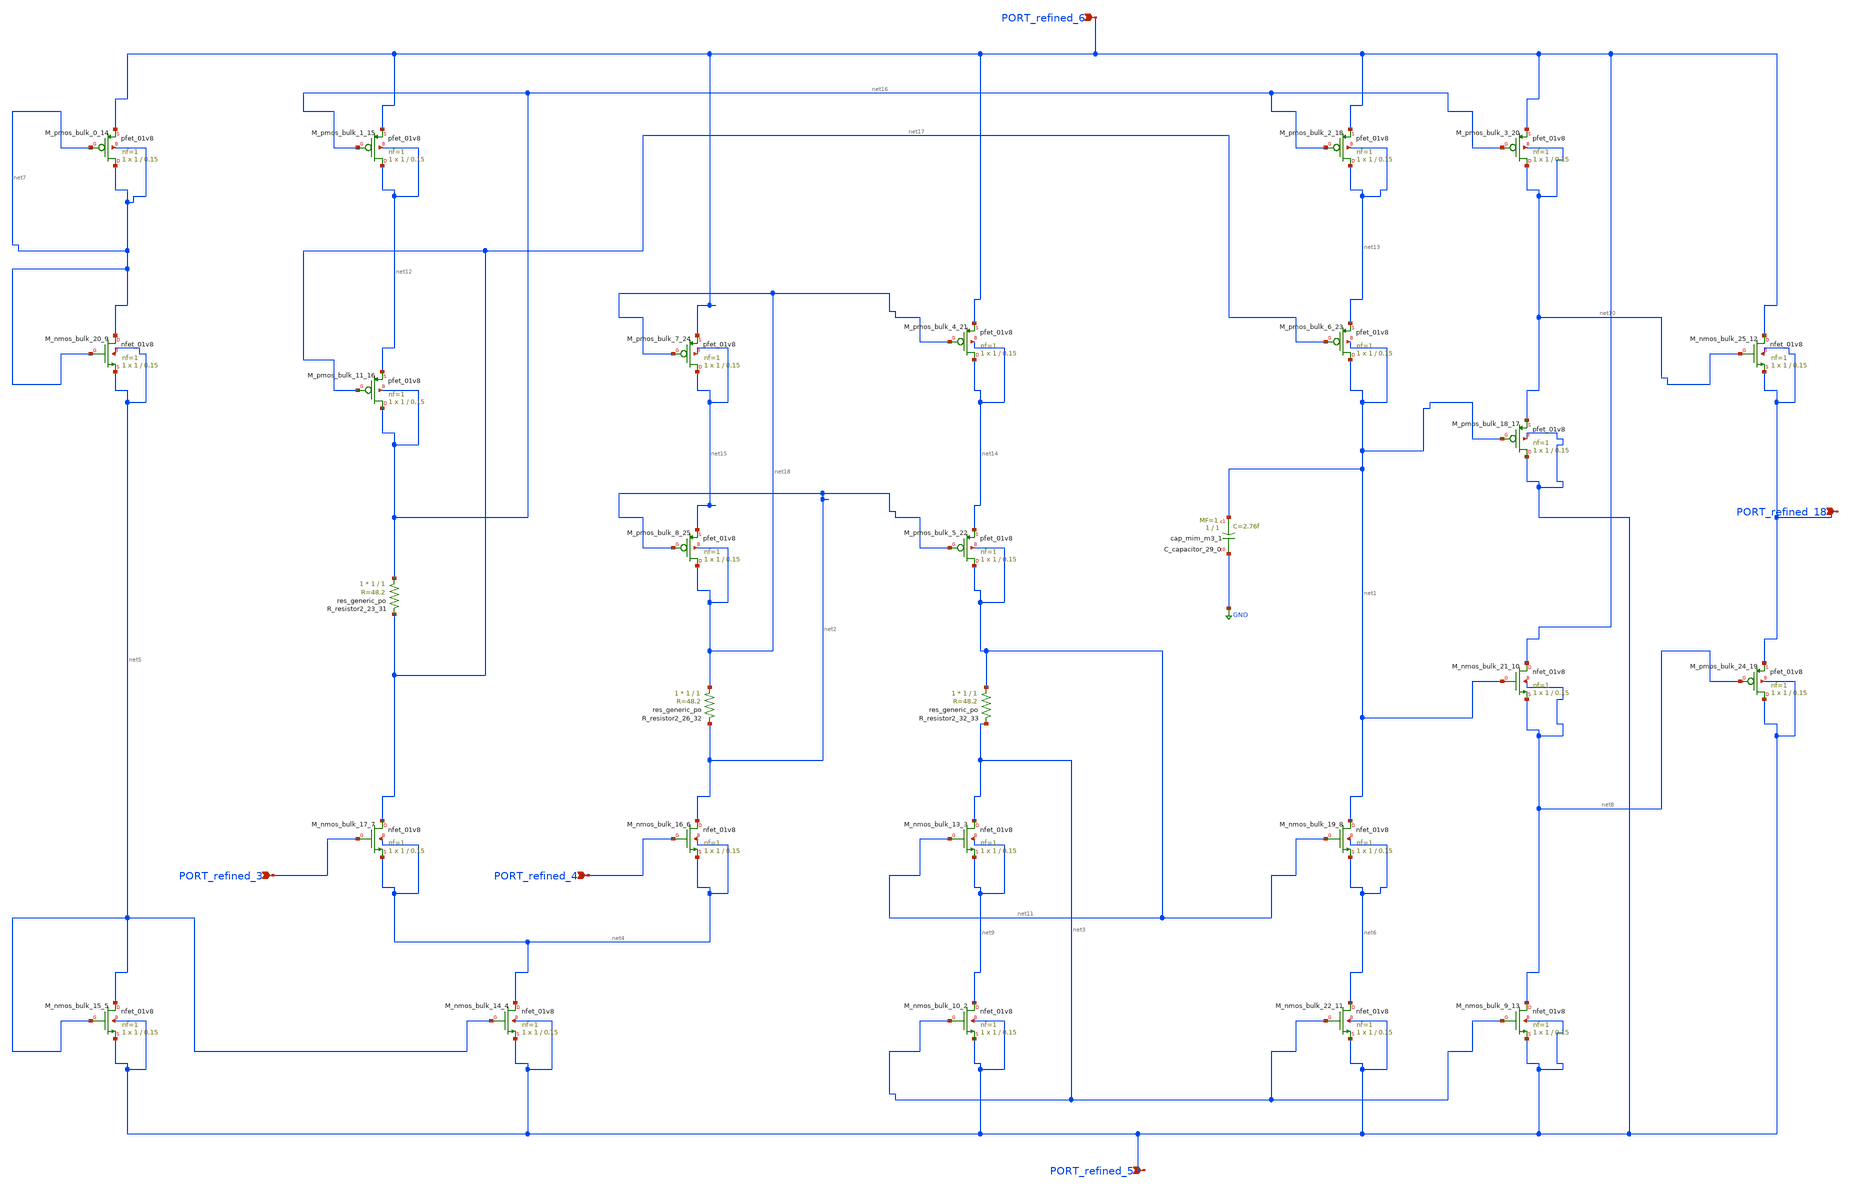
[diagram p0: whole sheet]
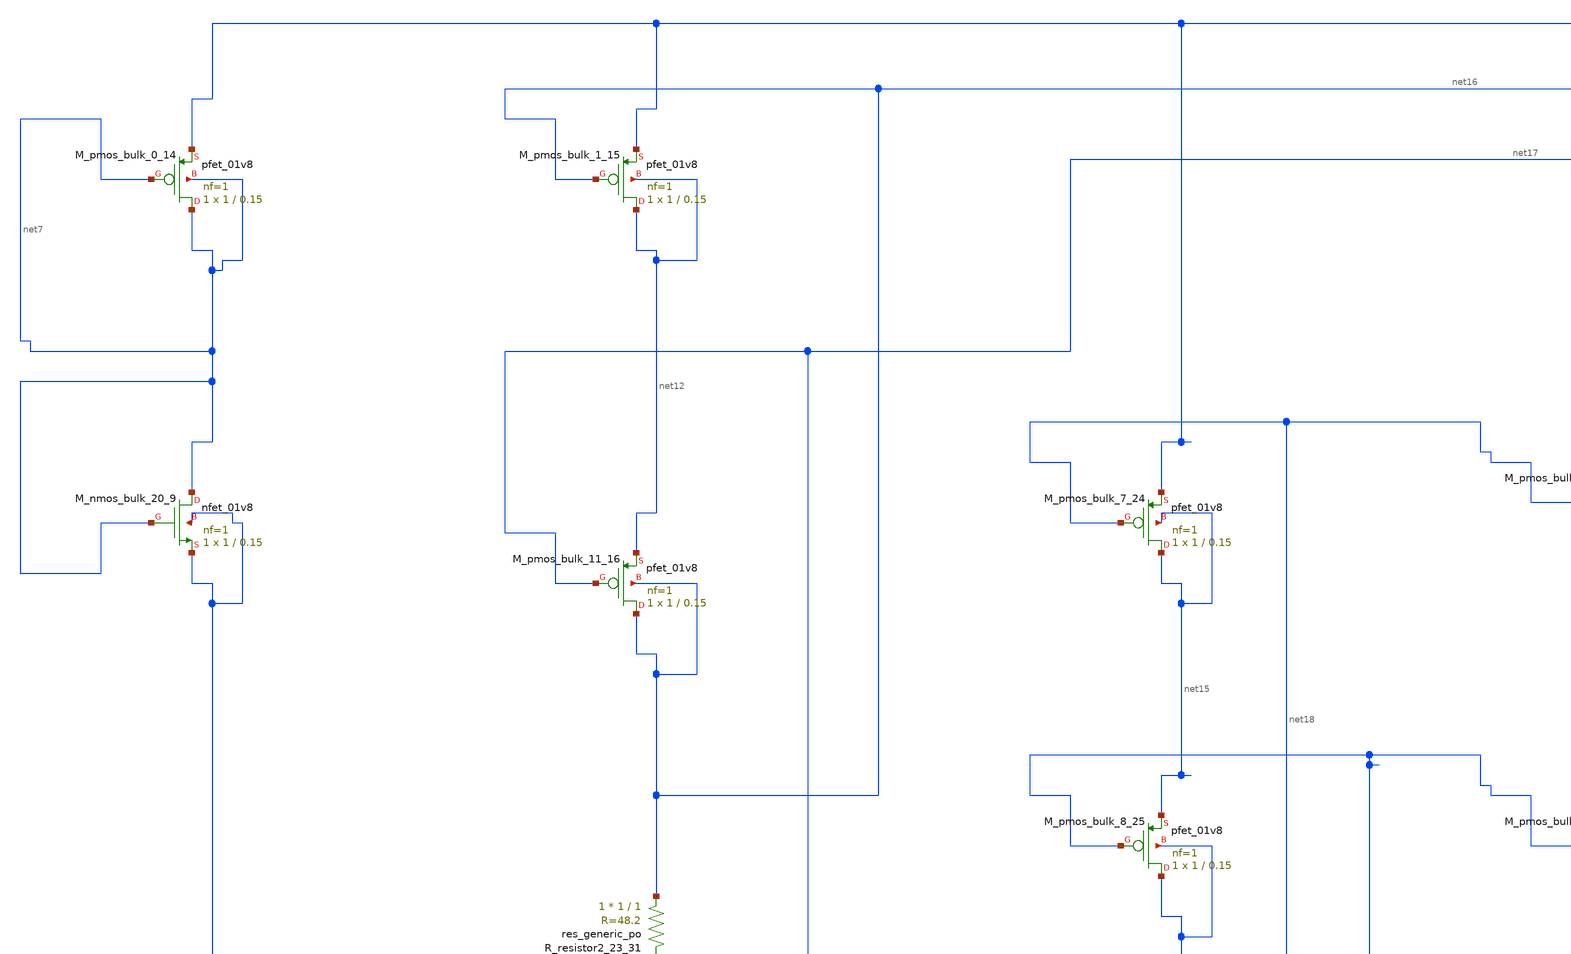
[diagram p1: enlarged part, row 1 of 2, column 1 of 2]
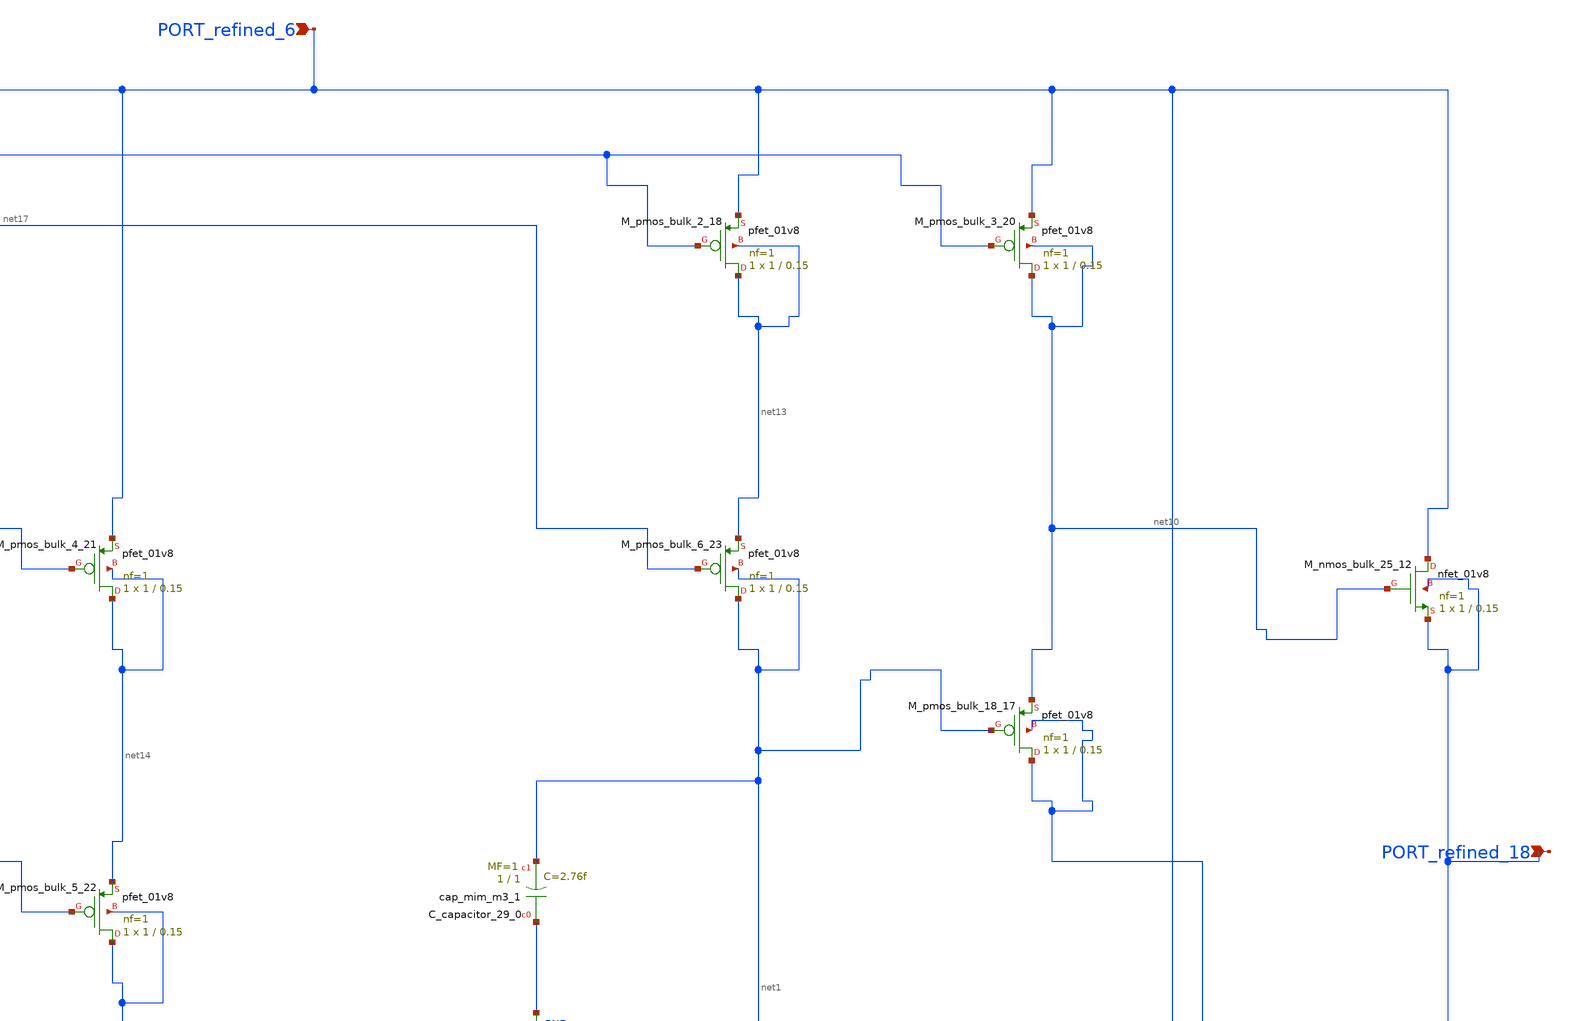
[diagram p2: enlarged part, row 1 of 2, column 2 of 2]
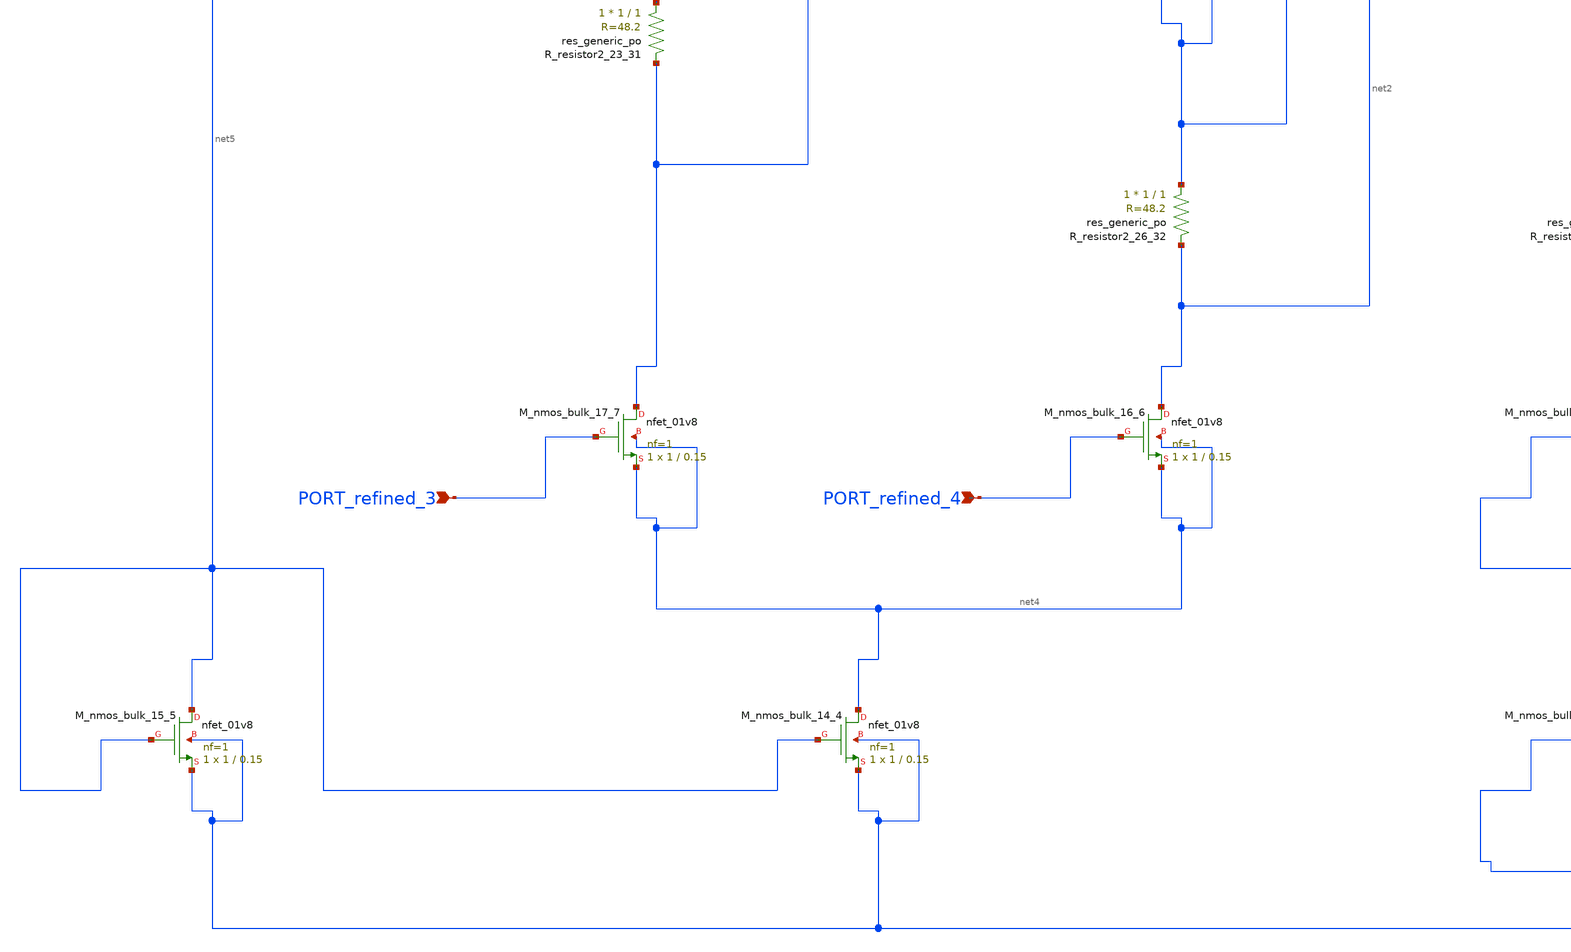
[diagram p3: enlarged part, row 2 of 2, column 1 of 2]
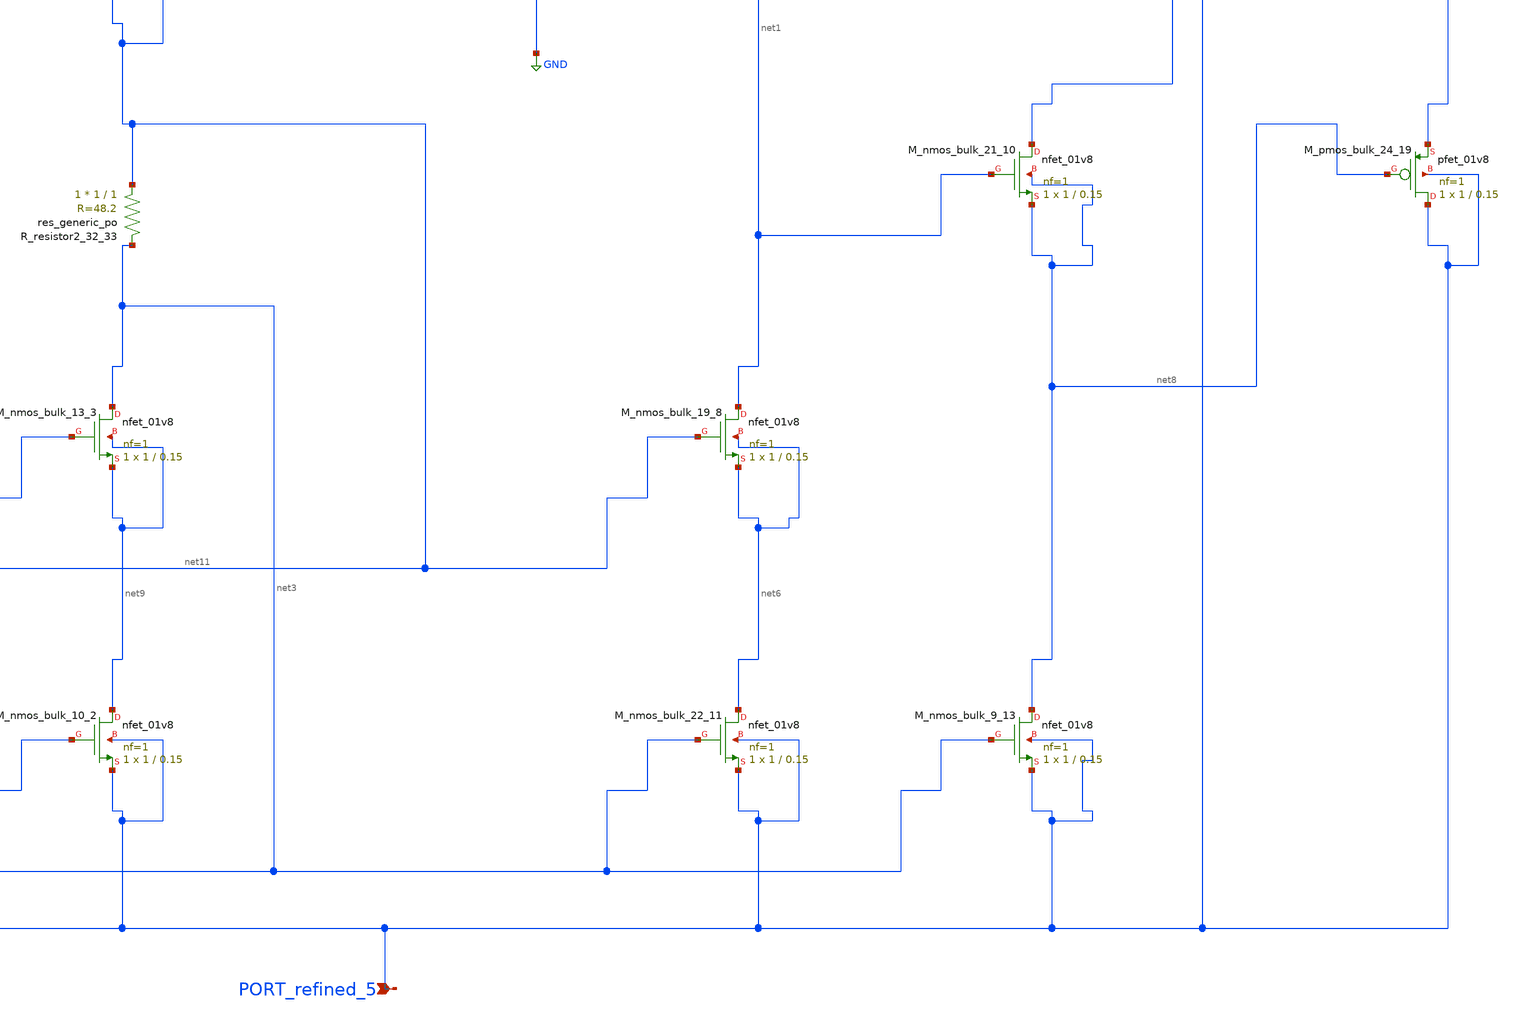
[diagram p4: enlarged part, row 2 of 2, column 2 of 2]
** sch_path: schematics/10_1007_s40747-016-0027-3_04_002.sch
**.subckt 10_1007_s40747-016-0027-3_04_002 PORT_refined_18 PORT_refined_3 PORT_refined_4
*+ PORT_refined_5 PORT_refined_6
*.ipin PORT_refined_18
*.ipin PORT_refined_3
*.ipin PORT_refined_4
*.ipin PORT_refined_5
*.ipin PORT_refined_6
XC_capacitor_29_0 GND net1 sky130_fd_pr__cap_mim_m3_1 W=1 L=1 MF=1 m=1
XM_nmos_bulk_10_2 net9 net3 PORT_refined_5 PORT_refined_5 sky130_fd_pr__nfet_01v8 L=0.15 W=1 nf=1 ad='int((1 + 1)/2) * 1 / 1 * 0.29'
+ as='int((1 + 2)/2) * 1 / 1 * 0.29' pd='2*int((1 + 1)/2) * (1 / 1 + 0.29)' ps='2*int((1 + 2)/2) * (1 / 1 + 0.29)'
+ nrd='0.29 / 1 ' nrs='0.29 / 1 ' sa=0 sb=0 sd=0 mult=1 m=1
XM_nmos_bulk_13_3 net3 net11 net9 net9 sky130_fd_pr__nfet_01v8 L=0.15 W=1 nf=1 ad='int((1 + 1)/2) * 1 / 1 * 0.29'
+ as='int((1 + 2)/2) * 1 / 1 * 0.29' pd='2*int((1 + 1)/2) * (1 / 1 + 0.29)' ps='2*int((1 + 2)/2) * (1 / 1 + 0.29)'
+ nrd='0.29 / 1 ' nrs='0.29 / 1 ' sa=0 sb=0 sd=0 mult=1 m=1
XM_nmos_bulk_14_4 net4 net5 PORT_refined_5 PORT_refined_5 sky130_fd_pr__nfet_01v8 L=0.15 W=1 nf=1 ad='int((1 + 1)/2) * 1 / 1 * 0.29'
+ as='int((1 + 2)/2) * 1 / 1 * 0.29' pd='2*int((1 + 1)/2) * (1 / 1 + 0.29)' ps='2*int((1 + 2)/2) * (1 / 1 + 0.29)'
+ nrd='0.29 / 1 ' nrs='0.29 / 1 ' sa=0 sb=0 sd=0 mult=1 m=1
XM_nmos_bulk_15_5 net5 net5 PORT_refined_5 PORT_refined_5 sky130_fd_pr__nfet_01v8 L=0.15 W=1 nf=1 ad='int((1 + 1)/2) * 1 / 1 * 0.29'
+ as='int((1 + 2)/2) * 1 / 1 * 0.29' pd='2*int((1 + 1)/2) * (1 / 1 + 0.29)' ps='2*int((1 + 2)/2) * (1 / 1 + 0.29)'
+ nrd='0.29 / 1 ' nrs='0.29 / 1 ' sa=0 sb=0 sd=0 mult=1 m=1
XM_nmos_bulk_16_6 net2 PORT_refined_4 net4 net4 sky130_fd_pr__nfet_01v8 L=0.15 W=1 nf=1 ad='int((1 + 1)/2) * 1 / 1 * 0.29'
+ as='int((1 + 2)/2) * 1 / 1 * 0.29' pd='2*int((1 + 1)/2) * (1 / 1 + 0.29)' ps='2*int((1 + 2)/2) * (1 / 1 + 0.29)'
+ nrd='0.29 / 1 ' nrs='0.29 / 1 ' sa=0 sb=0 sd=0 mult=1 m=1
XM_nmos_bulk_17_7 net17 PORT_refined_3 net4 net4 sky130_fd_pr__nfet_01v8 L=0.15 W=1 nf=1 ad='int((1 + 1)/2) * 1 / 1 * 0.29'
+ as='int((1 + 2)/2) * 1 / 1 * 0.29' pd='2*int((1 + 1)/2) * (1 / 1 + 0.29)' ps='2*int((1 + 2)/2) * (1 / 1 + 0.29)'
+ nrd='0.29 / 1 ' nrs='0.29 / 1 ' sa=0 sb=0 sd=0 mult=1 m=1
XM_nmos_bulk_19_8 net1 net11 net6 net6 sky130_fd_pr__nfet_01v8 L=0.15 W=1 nf=1 ad='int((1 + 1)/2) * 1 / 1 * 0.29'
+ as='int((1 + 2)/2) * 1 / 1 * 0.29' pd='2*int((1 + 1)/2) * (1 / 1 + 0.29)' ps='2*int((1 + 2)/2) * (1 / 1 + 0.29)'
+ nrd='0.29 / 1 ' nrs='0.29 / 1 ' sa=0 sb=0 sd=0 mult=1 m=1
XM_nmos_bulk_20_9 net7 net7 net5 net5 sky130_fd_pr__nfet_01v8 L=0.15 W=1 nf=1 ad='int((1 + 1)/2) * 1 / 1 * 0.29'
+ as='int((1 + 2)/2) * 1 / 1 * 0.29' pd='2*int((1 + 1)/2) * (1 / 1 + 0.29)' ps='2*int((1 + 2)/2) * (1 / 1 + 0.29)'
+ nrd='0.29 / 1 ' nrs='0.29 / 1 ' sa=0 sb=0 sd=0 mult=1 m=1
XM_nmos_bulk_21_10 PORT_refined_6 net1 net8 net8 sky130_fd_pr__nfet_01v8 L=0.15 W=1 nf=1 ad='int((1 + 1)/2) * 1 / 1 * 0.29'
+ as='int((1 + 2)/2) * 1 / 1 * 0.29' pd='2*int((1 + 1)/2) * (1 / 1 + 0.29)' ps='2*int((1 + 2)/2) * (1 / 1 + 0.29)'
+ nrd='0.29 / 1 ' nrs='0.29 / 1 ' sa=0 sb=0 sd=0 mult=1 m=1
XM_nmos_bulk_22_11 net6 net3 PORT_refined_5 PORT_refined_5 sky130_fd_pr__nfet_01v8 L=0.15 W=1 nf=1 ad='int((1 + 1)/2) * 1 / 1 * 0.29'
+ as='int((1 + 2)/2) * 1 / 1 * 0.29' pd='2*int((1 + 1)/2) * (1 / 1 + 0.29)' ps='2*int((1 + 2)/2) * (1 / 1 + 0.29)'
+ nrd='0.29 / 1 ' nrs='0.29 / 1 ' sa=0 sb=0 sd=0 mult=1 m=1
XM_nmos_bulk_25_12 PORT_refined_6 net10 PORT_refined_18 PORT_refined_18 sky130_fd_pr__nfet_01v8 L=0.15
+ W=1 nf=1 ad='int((1 + 1)/2) * 1 / 1 * 0.29' as='int((1 + 2)/2) * 1 / 1 * 0.29' pd='2*int((1 + 1)/2) * (1 / 1 + 0.29)'
+ ps='2*int((1 + 2)/2) * (1 / 1 + 0.29)' nrd='0.29 / 1 ' nrs='0.29 / 1 ' sa=0 sb=0 sd=0 mult=1 m=1
XM_nmos_bulk_9_13 net8 net3 PORT_refined_5 PORT_refined_5 sky130_fd_pr__nfet_01v8 L=0.15 W=1 nf=1 ad='int((1 + 1)/2) * 1 / 1 * 0.29'
+ as='int((1 + 2)/2) * 1 / 1 * 0.29' pd='2*int((1 + 1)/2) * (1 / 1 + 0.29)' ps='2*int((1 + 2)/2) * (1 / 1 + 0.29)'
+ nrd='0.29 / 1 ' nrs='0.29 / 1 ' sa=0 sb=0 sd=0 mult=1 m=1
XM_pmos_bulk_0_14 net7 net7 PORT_refined_6 net7 sky130_fd_pr__pfet_01v8 L=0.15 W=1 nf=1 ad='int((1 + 1)/2) * 1 / 1 * 0.29'
+ as='int((1 + 2)/2) * 1 / 1 * 0.29' pd='2*int((1 + 1)/2) * (1 / 1 + 0.29)' ps='2*int((1 + 2)/2) * (1 / 1 + 0.29)'
+ nrd='0.29 / 1 ' nrs='0.29 / 1 ' sa=0 sb=0 sd=0 mult=1 m=1
XM_pmos_bulk_1_15 net12 net16 PORT_refined_6 net12 sky130_fd_pr__pfet_01v8 L=0.15 W=1 nf=1 ad='int((1 + 1)/2) * 1 / 1 * 0.29'
+ as='int((1 + 2)/2) * 1 / 1 * 0.29' pd='2*int((1 + 1)/2) * (1 / 1 + 0.29)' ps='2*int((1 + 2)/2) * (1 / 1 + 0.29)'
+ nrd='0.29 / 1 ' nrs='0.29 / 1 ' sa=0 sb=0 sd=0 mult=1 m=1
XM_pmos_bulk_11_16 net16 net17 net12 net16 sky130_fd_pr__pfet_01v8 L=0.15 W=1 nf=1 ad='int((1 + 1)/2) * 1 / 1 * 0.29'
+ as='int((1 + 2)/2) * 1 / 1 * 0.29' pd='2*int((1 + 1)/2) * (1 / 1 + 0.29)' ps='2*int((1 + 2)/2) * (1 / 1 + 0.29)'
+ nrd='0.29 / 1 ' nrs='0.29 / 1 ' sa=0 sb=0 sd=0 mult=1 m=1
XM_pmos_bulk_18_17 PORT_refined_5 net1 net10 PORT_refined_5 sky130_fd_pr__pfet_01v8 L=0.15 W=1 nf=1 ad='int((1 + 1)/2) * 1 / 1 * 0.29'
+ as='int((1 + 2)/2) * 1 / 1 * 0.29' pd='2*int((1 + 1)/2) * (1 / 1 + 0.29)' ps='2*int((1 + 2)/2) * (1 / 1 + 0.29)'
+ nrd='0.29 / 1 ' nrs='0.29 / 1 ' sa=0 sb=0 sd=0 mult=1 m=1
XM_pmos_bulk_2_18 net13 net16 PORT_refined_6 net13 sky130_fd_pr__pfet_01v8 L=0.15 W=1 nf=1 ad='int((1 + 1)/2) * 1 / 1 * 0.29'
+ as='int((1 + 2)/2) * 1 / 1 * 0.29' pd='2*int((1 + 1)/2) * (1 / 1 + 0.29)' ps='2*int((1 + 2)/2) * (1 / 1 + 0.29)'
+ nrd='0.29 / 1 ' nrs='0.29 / 1 ' sa=0 sb=0 sd=0 mult=1 m=1
XM_pmos_bulk_24_19 PORT_refined_5 net8 PORT_refined_18 PORT_refined_5 sky130_fd_pr__pfet_01v8 L=0.15
+ W=1 nf=1 ad='int((1 + 1)/2) * 1 / 1 * 0.29' as='int((1 + 2)/2) * 1 / 1 * 0.29' pd='2*int((1 + 1)/2) * (1 / 1 + 0.29)'
+ ps='2*int((1 + 2)/2) * (1 / 1 + 0.29)' nrd='0.29 / 1 ' nrs='0.29 / 1 ' sa=0 sb=0 sd=0 mult=1 m=1
XM_pmos_bulk_3_20 net10 net16 PORT_refined_6 net10 sky130_fd_pr__pfet_01v8 L=0.15 W=1 nf=1 ad='int((1 + 1)/2) * 1 / 1 * 0.29'
+ as='int((1 + 2)/2) * 1 / 1 * 0.29' pd='2*int((1 + 1)/2) * (1 / 1 + 0.29)' ps='2*int((1 + 2)/2) * (1 / 1 + 0.29)'
+ nrd='0.29 / 1 ' nrs='0.29 / 1 ' sa=0 sb=0 sd=0 mult=1 m=1
XM_pmos_bulk_4_21 net14 net18 PORT_refined_6 net14 sky130_fd_pr__pfet_01v8 L=0.15 W=1 nf=1 ad='int((1 + 1)/2) * 1 / 1 * 0.29'
+ as='int((1 + 2)/2) * 1 / 1 * 0.29' pd='2*int((1 + 1)/2) * (1 / 1 + 0.29)' ps='2*int((1 + 2)/2) * (1 / 1 + 0.29)'
+ nrd='0.29 / 1 ' nrs='0.29 / 1 ' sa=0 sb=0 sd=0 mult=1 m=1
XM_pmos_bulk_5_22 net11 net2 net14 net11 sky130_fd_pr__pfet_01v8 L=0.15 W=1 nf=1 ad='int((1 + 1)/2) * 1 / 1 * 0.29'
+ as='int((1 + 2)/2) * 1 / 1 * 0.29' pd='2*int((1 + 1)/2) * (1 / 1 + 0.29)' ps='2*int((1 + 2)/2) * (1 / 1 + 0.29)'
+ nrd='0.29 / 1 ' nrs='0.29 / 1 ' sa=0 sb=0 sd=0 mult=1 m=1
XM_pmos_bulk_6_23 net1 net17 net13 net1 sky130_fd_pr__pfet_01v8 L=0.15 W=1 nf=1 ad='int((1 + 1)/2) * 1 / 1 * 0.29'
+ as='int((1 + 2)/2) * 1 / 1 * 0.29' pd='2*int((1 + 1)/2) * (1 / 1 + 0.29)' ps='2*int((1 + 2)/2) * (1 / 1 + 0.29)'
+ nrd='0.29 / 1 ' nrs='0.29 / 1 ' sa=0 sb=0 sd=0 mult=1 m=1
XM_pmos_bulk_7_24 net15 net18 PORT_refined_6 net15 sky130_fd_pr__pfet_01v8 L=0.15 W=1 nf=1 ad='int((1 + 1)/2) * 1 / 1 * 0.29'
+ as='int((1 + 2)/2) * 1 / 1 * 0.29' pd='2*int((1 + 1)/2) * (1 / 1 + 0.29)' ps='2*int((1 + 2)/2) * (1 / 1 + 0.29)'
+ nrd='0.29 / 1 ' nrs='0.29 / 1 ' sa=0 sb=0 sd=0 mult=1 m=1
XM_pmos_bulk_8_25 net18 net2 net15 net18 sky130_fd_pr__pfet_01v8 L=0.15 W=1 nf=1 ad='int((1 + 1)/2) * 1 / 1 * 0.29'
+ as='int((1 + 2)/2) * 1 / 1 * 0.29' pd='2*int((1 + 1)/2) * (1 / 1 + 0.29)' ps='2*int((1 + 2)/2) * (1 / 1 + 0.29)'
+ nrd='0.29 / 1 ' nrs='0.29 / 1 ' sa=0 sb=0 sd=0 mult=1 m=1
XR_resistor2_23_31 net16 net17 sky130_fd_pr__res_generic_po W=1 L=1 m=1
XR_resistor2_26_32 net18 net2 sky130_fd_pr__res_generic_po W=1 L=1 m=1
XR_resistor2_32_33 net11 net3 sky130_fd_pr__res_generic_po W=1 L=1 m=1
**.ends
.GLOBAL GND
.end
